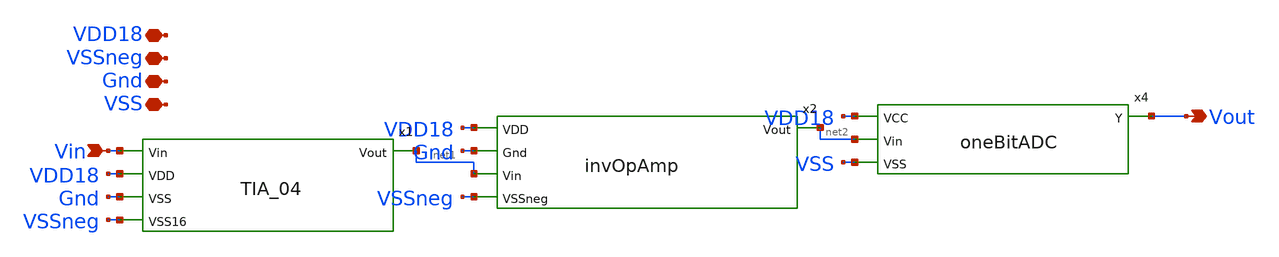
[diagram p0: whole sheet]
** sch_path: xschem/1LineSelectOutput04.sch
**.subckt 1LineSelectOutput04 Vin VDD18 Vout VSSneg Gnd VSS
*.ipin Vin
*.iopin VDD18
*.opin Vout
*.iopin VSSneg
*.iopin Gnd
*.iopin VSS
x4 VDD18 Vout net2 VSS oneBitADC
x2 net2 VDD18 Gnd net1 VSSneg invOpAmp
x1 Vin VDD18 net1 Gnd VSSneg TIA_04
**.ends
.end
